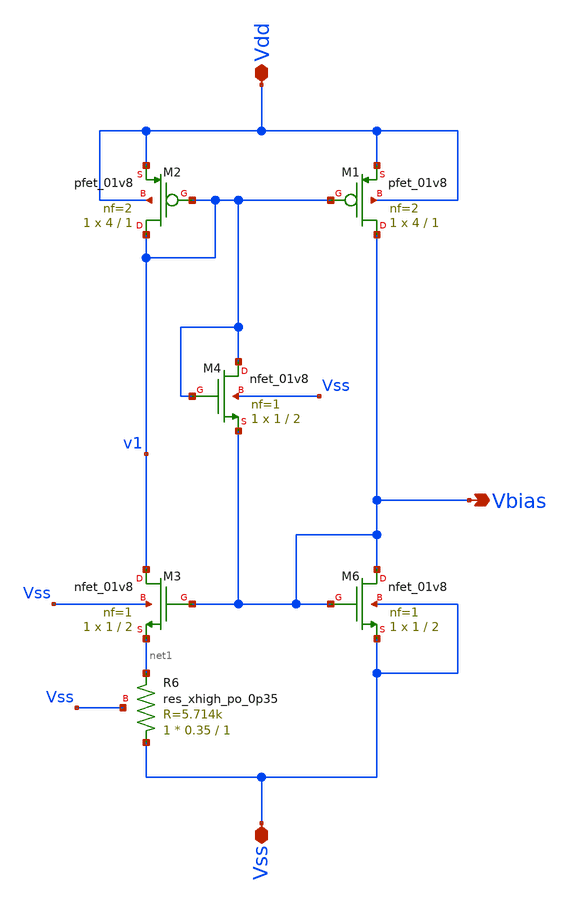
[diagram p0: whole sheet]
** sch_path: Circuits/Examples/OpAmp/GmBias.sch
**.subckt GmBias Vbias Vss Vdd
*.opin Vbias
*.iopin Vss
*.iopin Vdd
XM6 Vbias Vbias Vss Vss sky130_fd_pr__nfet_01v8 L=2 W=1 nf=1 ad='int((nf+1)/2) * W/nf * 0.29' as='int((nf+2)/2) * W/nf * 0.29'
+ pd='2*int((nf+1)/2) * (W/nf + 0.29)' ps='2*int((nf+2)/2) * (W/nf + 0.29)' nrd='0.29 / W' nrs='0.29 / W'
+ sa=0 sb=0 sd=0 mult=1 m=1
XM2 v1 v1 Vdd Vdd sky130_fd_pr__pfet_01v8 L=1 W=4 nf=2 ad='int((nf+1)/2) * W/nf * 0.29' as='int((nf+2)/2) * W/nf * 0.29'
+ pd='2*int((nf+1)/2) * (W/nf + 0.29)' ps='2*int((nf+2)/2) * (W/nf + 0.29)' nrd='0.29 / W' nrs='0.29 / W'
+ sa=0 sb=0 sd=0 mult=1 m=1
XM1 Vbias v1 Vdd Vdd sky130_fd_pr__pfet_01v8 L=1 W=4 nf=2 ad='int((nf+1)/2) * W/nf * 0.29' as='int((nf+2)/2) * W/nf * 0.29'
+ pd='2*int((nf+1)/2) * (W/nf + 0.29)' ps='2*int((nf+2)/2) * (W/nf + 0.29)' nrd='0.29 / W' nrs='0.29 / W'
+ sa=0 sb=0 sd=0 mult=1 m=1
XM3 v1 Vbias net1 Vss sky130_fd_pr__nfet_01v8 L=2 W=1 nf=1 ad='int((nf+1)/2) * W/nf * 0.29' as='int((nf+2)/2) * W/nf * 0.29'
+ pd='2*int((nf+1)/2) * (W/nf + 0.29)' ps='2*int((nf+2)/2) * (W/nf + 0.29)' nrd='0.29 / W' nrs='0.29 / W'
+ sa=0 sb=0 sd=0 mult=1 m=1
XR6 Vss net1 Vss sky130_fd_pr__res_xhigh_po_0p35 L=1 mult=1 m=1
XM4 v1 v1 Vbias Vss sky130_fd_pr__nfet_01v8 L=2 W=1 nf=1 ad='int((nf+1)/2) * W/nf * 0.29' as='int((nf+2)/2) * W/nf * 0.29'
+ pd='2*int((nf+1)/2) * (W/nf + 0.29)' ps='2*int((nf+2)/2) * (W/nf + 0.29)' nrd='0.29 / W' nrs='0.29 / W'
+ sa=0 sb=0 sd=0 mult=1 m=1
**.ends
.end
